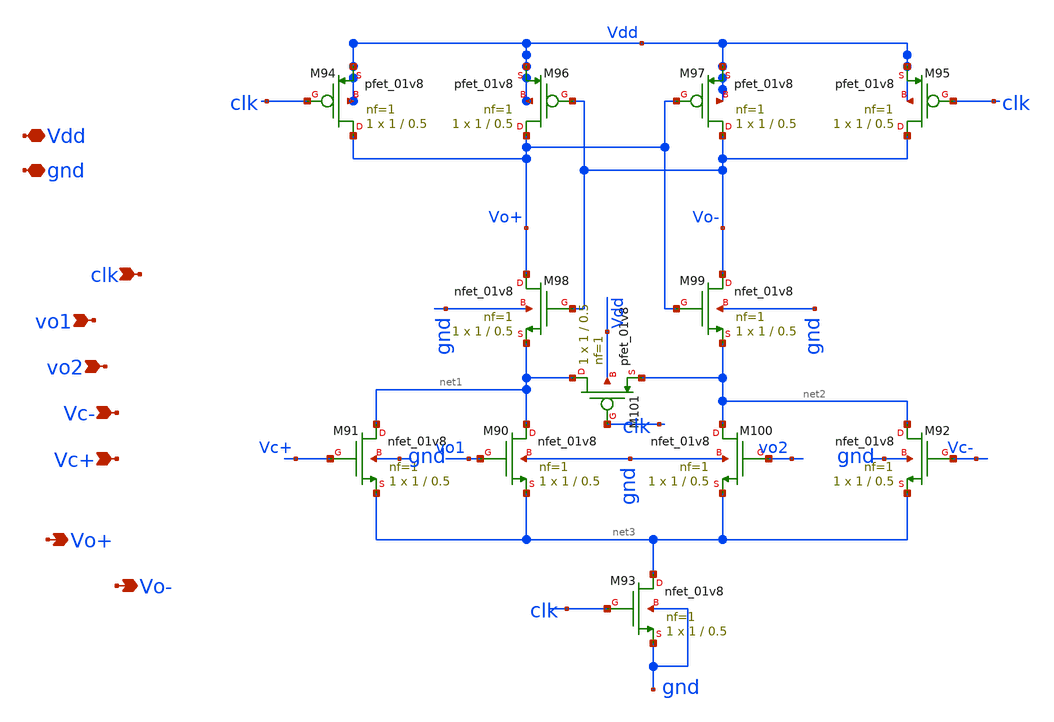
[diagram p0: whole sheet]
** sch_path: xschem/charge_pumps2/comparator_lvs.sch
**.subckt comparator_lvs gnd Vdd vo1 vo2 Vc- Vc+ Vo+ Vo- clk
*.iopin gnd
*.iopin Vdd
*.ipin vo1
*.ipin vo2
*.ipin Vc-
*.ipin Vc+
*.opin Vo+
*.opin Vo-
*.ipin clk
XM90 net1 vo1 net3 gnd sky130_fd_pr__nfet_01v8 L=0.5 W=1 nf=1 ad='int((nf+1)/2) * W/nf * 0.29' as='int((nf+2)/2) * W/nf * 0.29'
+ pd='2*int((nf+1)/2) * (W/nf + 0.29)' ps='2*int((nf+2)/2) * (W/nf + 0.29)' nrd='0.29 / W' nrs='0.29 / W'
+ sa=0 sb=0 sd=0 mult=1 m=1
XM91 net1 Vc+ net3 gnd sky130_fd_pr__nfet_01v8 L=0.5 W=1 nf=1 ad='int((nf+1)/2) * W/nf * 0.29' as='int((nf+2)/2) * W/nf * 0.29'
+ pd='2*int((nf+1)/2) * (W/nf + 0.29)' ps='2*int((nf+2)/2) * (W/nf + 0.29)' nrd='0.29 / W' nrs='0.29 / W'
+ sa=0 sb=0 sd=0 mult=1 m=1
XM92 net2 Vc- net3 gnd sky130_fd_pr__nfet_01v8 L=0.5 W=1 nf=1 ad='int((nf+1)/2) * W/nf * 0.29' as='int((nf+2)/2) * W/nf * 0.29'
+ pd='2*int((nf+1)/2) * (W/nf + 0.29)' ps='2*int((nf+2)/2) * (W/nf + 0.29)' nrd='0.29 / W' nrs='0.29 / W'
+ sa=0 sb=0 sd=0 mult=1 m=1
XM93 net3 clk gnd gnd sky130_fd_pr__nfet_01v8 L=0.5 W=1 nf=1 ad='int((nf+1)/2) * W/nf * 0.29' as='int((nf+2)/2) * W/nf * 0.29'
+ pd='2*int((nf+1)/2) * (W/nf + 0.29)' ps='2*int((nf+2)/2) * (W/nf + 0.29)' nrd='0.29 / W' nrs='0.29 / W'
+ sa=0 sb=0 sd=0 mult=1 m=1
XM94 Vo+ clk Vdd Vdd sky130_fd_pr__pfet_01v8 L=0.5 W=1 nf=1 ad='int((nf+1)/2) * W/nf * 0.29' as='int((nf+2)/2) * W/nf * 0.29'
+ pd='2*int((nf+1)/2) * (W/nf + 0.29)' ps='2*int((nf+2)/2) * (W/nf + 0.29)' nrd='0.29 / W' nrs='0.29 / W'
+ sa=0 sb=0 sd=0 mult=1 m=1
XM95 Vo- clk Vdd Vdd sky130_fd_pr__pfet_01v8 L=0.5 W=1 nf=1 ad='int((nf+1)/2) * W/nf * 0.29' as='int((nf+2)/2) * W/nf * 0.29'
+ pd='2*int((nf+1)/2) * (W/nf + 0.29)' ps='2*int((nf+2)/2) * (W/nf + 0.29)' nrd='0.29 / W' nrs='0.29 / W'
+ sa=0 sb=0 sd=0 mult=1 m=1
XM96 Vo+ Vo- Vdd Vdd sky130_fd_pr__pfet_01v8 L=0.5 W=1 nf=1 ad='int((nf+1)/2) * W/nf * 0.29' as='int((nf+2)/2) * W/nf * 0.29'
+ pd='2*int((nf+1)/2) * (W/nf + 0.29)' ps='2*int((nf+2)/2) * (W/nf + 0.29)' nrd='0.29 / W' nrs='0.29 / W'
+ sa=0 sb=0 sd=0 mult=1 m=1
XM97 Vo- Vo+ Vdd Vdd sky130_fd_pr__pfet_01v8 L=0.5 W=1 nf=1 ad='int((nf+1)/2) * W/nf * 0.29' as='int((nf+2)/2) * W/nf * 0.29'
+ pd='2*int((nf+1)/2) * (W/nf + 0.29)' ps='2*int((nf+2)/2) * (W/nf + 0.29)' nrd='0.29 / W' nrs='0.29 / W'
+ sa=0 sb=0 sd=0 mult=1 m=1
XM98 Vo+ Vo- net1 gnd sky130_fd_pr__nfet_01v8 L=0.5 W=1 nf=1 ad='int((nf+1)/2) * W/nf * 0.29' as='int((nf+2)/2) * W/nf * 0.29'
+ pd='2*int((nf+1)/2) * (W/nf + 0.29)' ps='2*int((nf+2)/2) * (W/nf + 0.29)' nrd='0.29 / W' nrs='0.29 / W'
+ sa=0 sb=0 sd=0 mult=1 m=1
XM99 Vo- Vo+ net2 gnd sky130_fd_pr__nfet_01v8 L=0.5 W=1 nf=1 ad='int((nf+1)/2) * W/nf * 0.29' as='int((nf+2)/2) * W/nf * 0.29'
+ pd='2*int((nf+1)/2) * (W/nf + 0.29)' ps='2*int((nf+2)/2) * (W/nf + 0.29)' nrd='0.29 / W' nrs='0.29 / W'
+ sa=0 sb=0 sd=0 mult=1 m=1
XM100 net2 vo2 net3 gnd sky130_fd_pr__nfet_01v8 L=0.5 W=1 nf=1 ad='int((nf+1)/2) * W/nf * 0.29' as='int((nf+2)/2) * W/nf * 0.29'
+ pd='2*int((nf+1)/2) * (W/nf + 0.29)' ps='2*int((nf+2)/2) * (W/nf + 0.29)' nrd='0.29 / W' nrs='0.29 / W'
+ sa=0 sb=0 sd=0 mult=1 m=1
XM101 net1 clk net2 Vdd sky130_fd_pr__pfet_01v8 L=0.5 W=1 nf=1 ad='int((nf+1)/2) * W/nf * 0.29' as='int((nf+2)/2) * W/nf * 0.29'
+ pd='2*int((nf+1)/2) * (W/nf + 0.29)' ps='2*int((nf+2)/2) * (W/nf + 0.29)' nrd='0.29 / W' nrs='0.29 / W'
+ sa=0 sb=0 sd=0 mult=1 m=1
**.ends
.end
